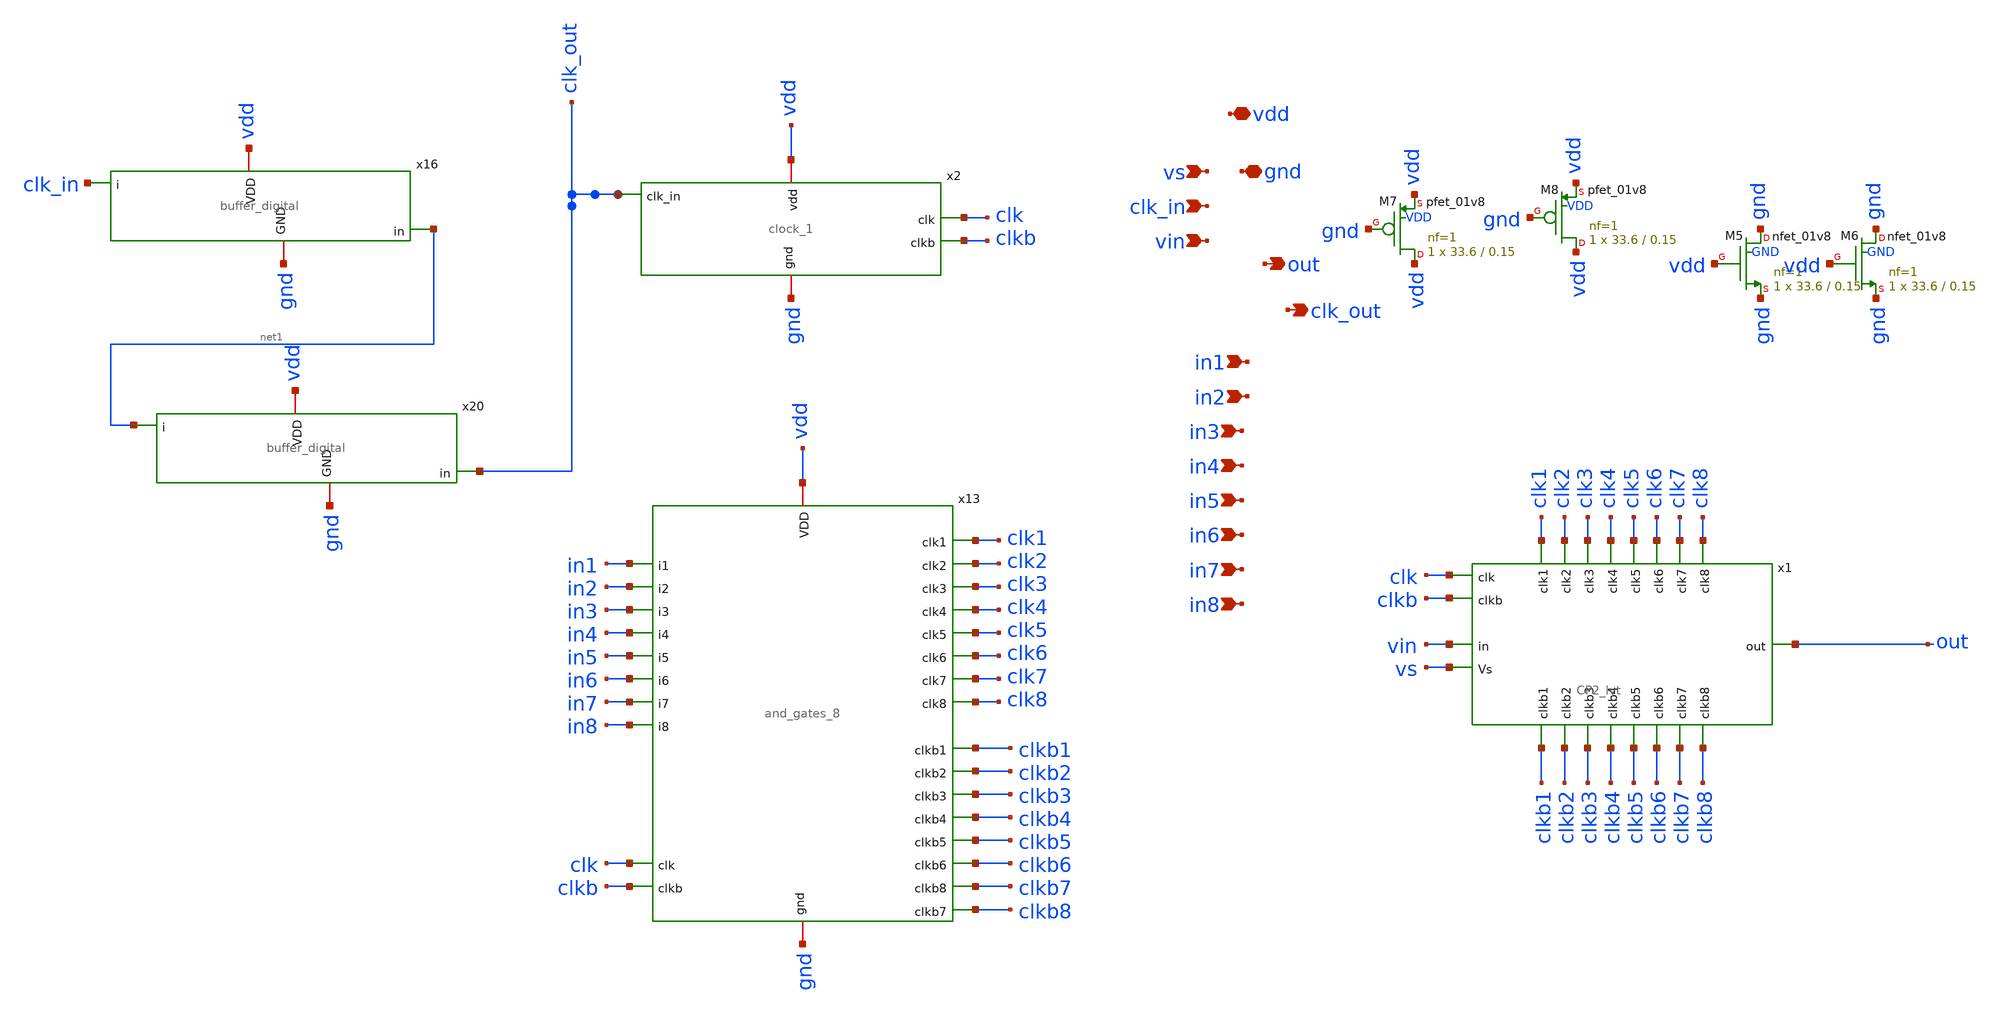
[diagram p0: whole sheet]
** sch_path: xschem/charge_pumps2/CP2_test.sch
**.subckt CP2_test clk_in vdd out vin vs gnd in1 in2 in3 in4 in5 in6 in7 in8 clk_out
*.ipin clk_in
*.iopin vdd
*.opin out
*.ipin vin
*.ipin vs
*.iopin gnd
*.ipin in1
*.ipin in2
*.ipin in3
*.ipin in4
*.ipin in5
*.ipin in6
*.ipin in7
*.ipin in8
*.opin clk_out
x1 clk3 clk5 clk4 clk1 clk2 clk6 clk clk8 clk7 vin out vs clkb4 clkb3 clkb2 clkb1 clkb8 clkb7 clkb6
+ clkb5 clkb CP2_lvt
XM5 gnd vdd gnd GND sky130_fd_pr__nfet_01v8 L=0.15 W=33.6 nf=1 ad='int((nf+1)/2) * W/nf * 0.29' as='int((nf+2)/2) * W/nf * 0.29'
+ pd='2*int((nf+1)/2) * (W/nf + 0.29)' ps='2*int((nf+2)/2) * (W/nf + 0.29)' nrd='0.29 / W' nrs='0.29 / W'
+ sa=0 sb=0 sd=0 mult=1 m=1
XM6 gnd vdd gnd GND sky130_fd_pr__nfet_01v8 L=0.15 W=33.6 nf=1 ad='int((nf+1)/2) * W/nf * 0.29' as='int((nf+2)/2) * W/nf * 0.29'
+ pd='2*int((nf+1)/2) * (W/nf + 0.29)' ps='2*int((nf+2)/2) * (W/nf + 0.29)' nrd='0.29 / W' nrs='0.29 / W'
+ sa=0 sb=0 sd=0 mult=1 m=1
XM7 vdd gnd vdd VDD sky130_fd_pr__pfet_01v8 L=0.15 W=33.6 nf=1 ad='int((nf+1)/2) * W/nf * 0.29' as='int((nf+2)/2) * W/nf * 0.29'
+ pd='2*int((nf+1)/2) * (W/nf + 0.29)' ps='2*int((nf+2)/2) * (W/nf + 0.29)' nrd='0.29 / W' nrs='0.29 / W'
+ sa=0 sb=0 sd=0 mult=1 m=1
XM8 vdd gnd vdd VDD sky130_fd_pr__pfet_01v8 L=0.15 W=33.6 nf=1 ad='int((nf+1)/2) * W/nf * 0.29' as='int((nf+2)/2) * W/nf * 0.29'
+ pd='2*int((nf+1)/2) * (W/nf + 0.29)' ps='2*int((nf+2)/2) * (W/nf + 0.29)' nrd='0.29 / W' nrs='0.29 / W'
+ sa=0 sb=0 sd=0 mult=1 m=1
x13 vdd clk clk1 clkb clkb1 clk2 clkb2 gnd in1 clkb4 clk4 in2 clk3 clkb3 in3 in4 in5 in6 in7 in8
+ clk5 clkb6 clk6 clkb5 clk7 clk8 clkb7 clkb8 and_gates_8
x2 clk_out clk clkb vdd gnd clock_1
x16 gnd vdd clk_in net1 buffer_digital
x20 gnd vdd net1 clk_out buffer_digital
**.ends
.end
